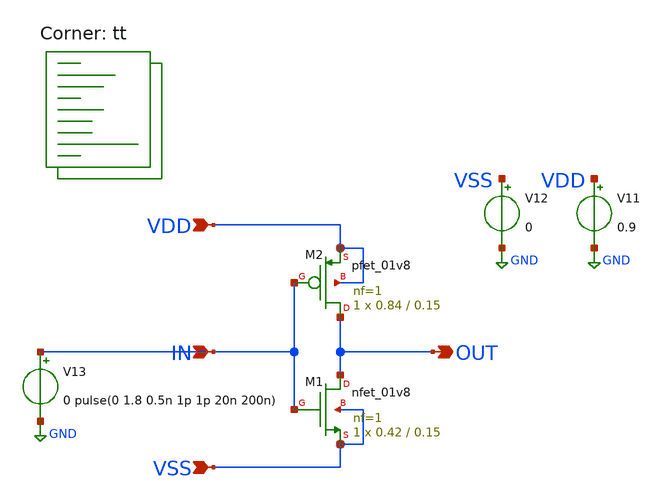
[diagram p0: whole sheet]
** sch_path: module/standard_cell_test/tb_inv.sch
**.subckt tb_inv IN VDD VSS OUT
*.ipin IN
*.ipin VDD
*.ipin VSS
*.opin OUT
XM1 OUT IN VSS VSS sky130_fd_pr__nfet_01v8 L=0.15 W=0.42 nf=1 ad='int((nf+1)/2) * W/nf * 0.29' as='int((nf+2)/2) * W/nf * 0.29'
+ pd='2*int((nf+1)/2) * (W/nf + 0.29)' ps='2*int((nf+2)/2) * (W/nf + 0.29)' nrd='0.29 / W' nrs='0.29 / W'
+ sa=0 sb=0 sd=0 mult=1 m=1
XM2 OUT IN VDD VDD sky130_fd_pr__pfet_01v8 L=0.15 W=0.84 nf=1 ad='int((nf+1)/2) * W/nf * 0.29' as='int((nf+2)/2) * W/nf * 0.29'
+ pd='2*int((nf+1)/2) * (W/nf + 0.29)' ps='2*int((nf+2)/2) * (W/nf + 0.29)' nrd='0.29 / W' nrs='0.29 / W'
+ sa=0 sb=0 sd=0 mult=1 m=1
V13 IN GND 0 pulse(0 1.8 0.5n 1p 1p 20n 200n)
V11 VDD GND 0.9
V12 VSS GND 0
**** begin user architecture code


.save all
.temp = 25
.tran 1p 1n
.OPTIONS savecurrents

.control
	run
        plot v(out) V(in)

.endc


.lib $::SKYWATER_MODELS/sky130.lib.spice tt
**** end user architecture code
**.ends
.GLOBAL GND
.end
